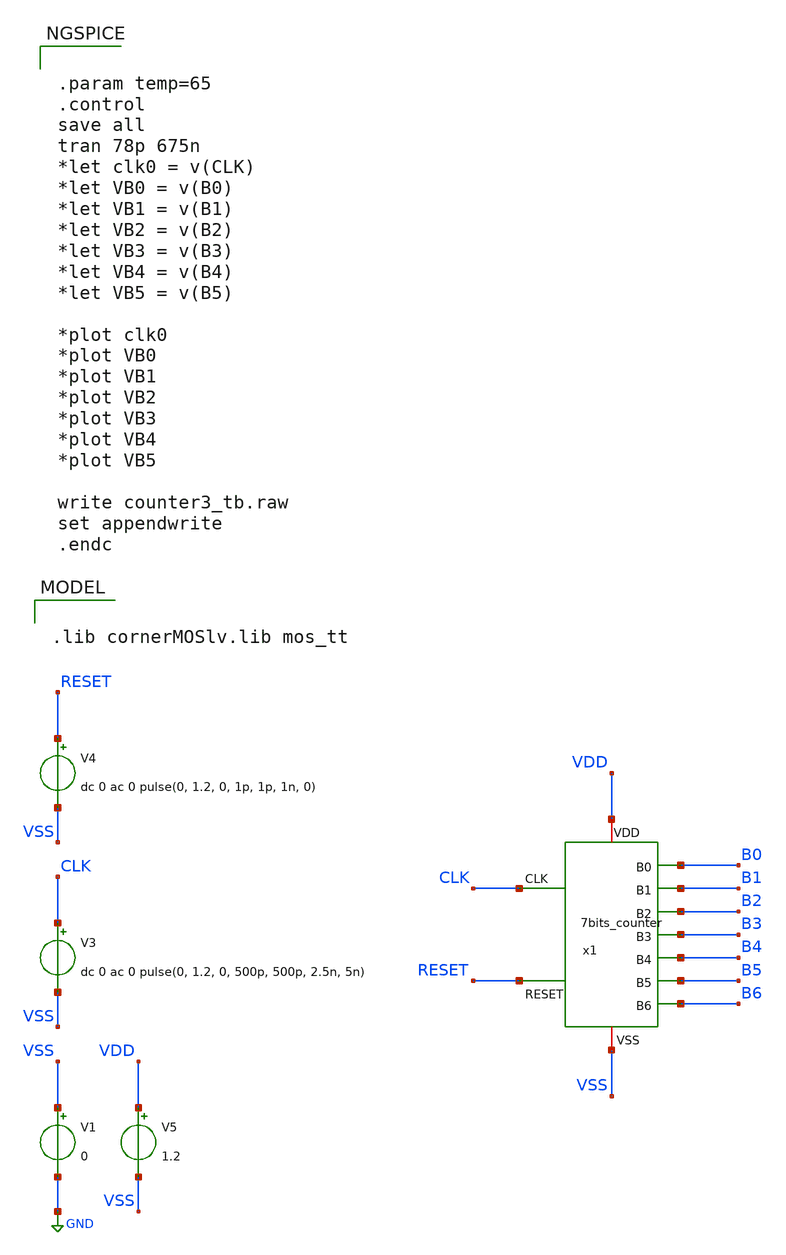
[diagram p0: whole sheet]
** sch_path: ADC8711-main/testbenches/tran/xschem/counter3_tb.sch
**.subckt counter3_tb
V1 VSS GND 0
V3 CLK VSS dc 0 ac 0 pulse(0, 1.2, 0, 500p, 500p, 2.5n, 5n)
V5 VDD VSS 1.2
V4 RESET VSS dc 0 ac 0 pulse(0, 1.2, 0, 1p, 1p, 1n, 0)
x1 B0 CLK VDD B1 B2 VSS RESET B3 B4 B5 B6 7bits_counter
**** begin user architecture code


.param temp=65
.control
save all
tran 78p 675n
*let clk0 = v(CLK)
*let VB0 = v(B0)
*let VB1 = v(B1)
*let VB2 = v(B2)
*let VB3 = v(B3)
*let VB4 = v(B4)
*let VB5 = v(B5)

*plot clk0
*plot VB0
*plot VB1
*plot VB2
*plot VB3
*plot VB4
*plot VB5

write counter3_tb.raw
set appendwrite
.endc



.lib cornerMOSlv.lib mos_tt

**** end user architecture code
**.ends
.GLOBAL GND
.end
